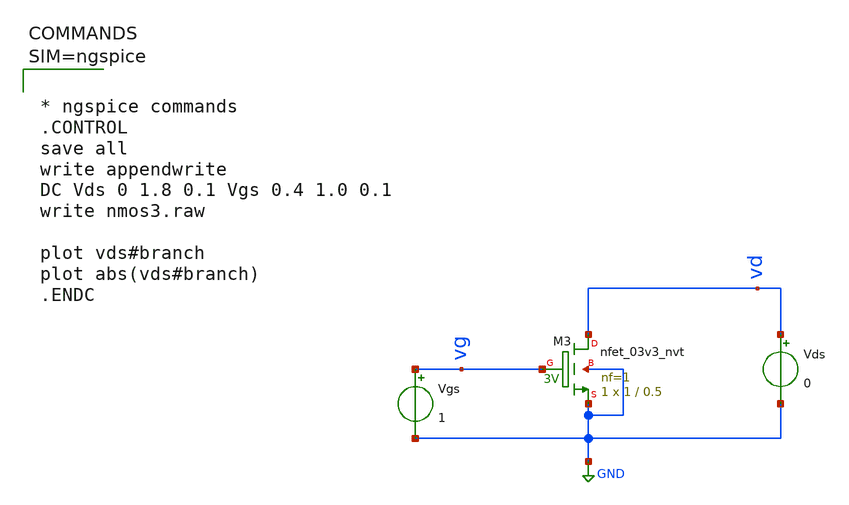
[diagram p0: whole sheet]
** sch_path: work/xschem/nmos3.sch
**.subckt nmos3
Vgs vg GND 1
Vds vd GND 0
XM3 vd vg GND GND sky130_fd_pr__nfet_03v3_nvt L=0.5 W=1 nf=1 ad='int((1 + 1)/2) * 1 / 1 * 0.29' as='int((1 + 2)/2) * 1 / 1 * 0.29'
+ pd='2*int((1 + 1)/2) * (1 / 1 + 0.29)' ps='2*int((1 + 2)/2) * (1 / 1 + 0.29)' nrd='0.29 / 1 ' nrs='0.29 / 1 '
+ sa=0 sb=0 sd=0 mult=1 m=1
**** begin user architecture code



* ngspice commands
.CONTROL
save all
write appendwrite
DC Vds 0 1.8 0.1 Vgs 0.4 1.0 0.1
write nmos3.raw

plot vds#branch
plot abs(vds#branch)
.ENDC




** opencircuitdesign pdks install
.lib $::SKYWATER_MODELS/sky130.lib.spice tt

**** end user architecture code
**.ends
.GLOBAL GND
.end
